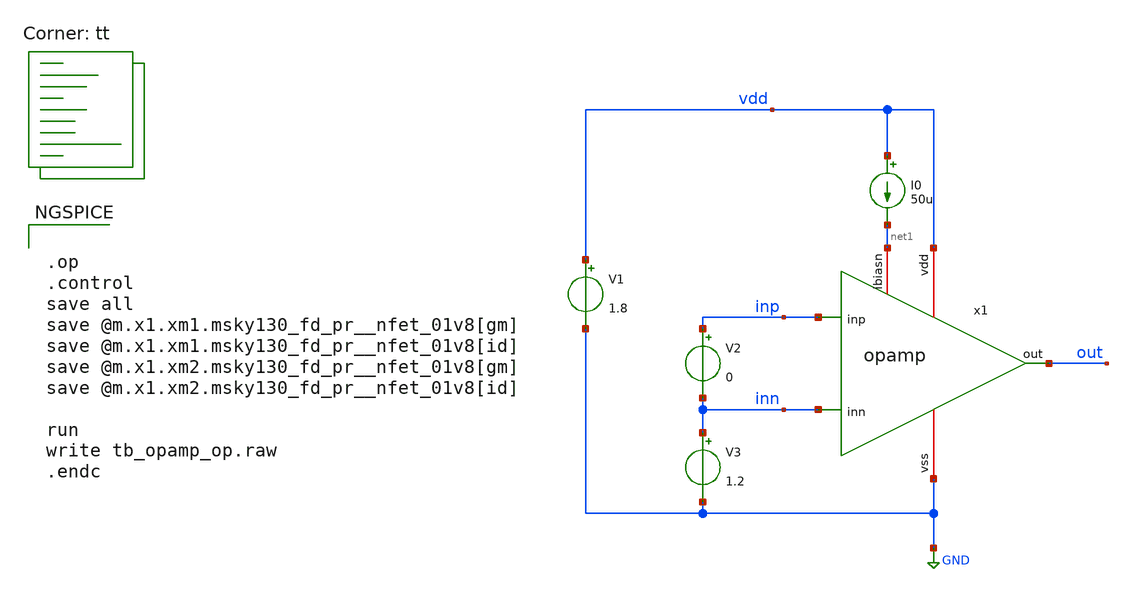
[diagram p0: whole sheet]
** sch_path: sky130A/HelloWorld/analog/schematic/tb_opamp_op.sch
**.subckt tb_opamp_op
x1 vdd out inp inn net1 GND opamp
V1 vdd GND 1.8
I0 vdd net1 50u
V2 inp inn 0
V3 inn GND 1.2
**** begin user architecture code
.lib $::SKYWATER_MODELS/sky130.lib.spice tt


.op
.control
save all
save @m.x1.xm1.msky130_fd_pr__nfet_01v8[gm]
save @m.x1.xm1.msky130_fd_pr__nfet_01v8[id]
save @m.x1.xm2.msky130_fd_pr__nfet_01v8[gm]
save @m.x1.xm2.msky130_fd_pr__nfet_01v8[id]

run
write tb_opamp_op.raw
.endc


**** end user architecture code
**.ends

* expanding   symbol:  opamp.sym # of pins=6
** sym_path: sky130A/HelloWorld/xschem/opamp.sym
** sch_path: sky130A/HelloWorld/xschem/opamp.sch
.subckt opamp vdd out inp inn ibiasn vss
*.ipin inn
*.ipin inp
*.iopin vdd
*.iopin vss
*.iopin ibiasn
*.opin out
XM1 pbias inn tail vss sky130_fd_pr__nfet_01v8 L=1 W=40 nf=1 ad='int((nf+1)/2) * W/nf * 0.29' as='int((nf+2)/2) * W/nf * 0.29'
+ pd='2*int((nf+1)/2) * (W/nf + 0.29)' ps='2*int((nf+2)/2) * (W/nf + 0.29)' nrd='0.29 / W' nrs='0.29 / W'
+ sa=0 sb=0 sd=0 mult=1 m=1
XM2 outz inp tail vss sky130_fd_pr__nfet_01v8 L=1 W=40 nf=1 ad='int((nf+1)/2) * W/nf * 0.29' as='int((nf+2)/2) * W/nf * 0.29'
+ pd='2*int((nf+1)/2) * (W/nf + 0.29)' ps='2*int((nf+2)/2) * (W/nf + 0.29)' nrd='0.29 / W' nrs='0.29 / W'
+ sa=0 sb=0 sd=0 mult=1 m=1
XM3 pbias pbias vdd vdd sky130_fd_pr__pfet_01v8 L=0.5 W=20 nf=1 ad='int((nf+1)/2) * W/nf * 0.29' as='int((nf+2)/2) * W/nf * 0.29'
+ pd='2*int((nf+1)/2) * (W/nf + 0.29)' ps='2*int((nf+2)/2) * (W/nf + 0.29)' nrd='0.29 / W' nrs='0.29 / W'
+ sa=0 sb=0 sd=0 mult=1 m=1
XM4 outz pbias vdd vdd sky130_fd_pr__pfet_01v8 L=0.5 W=20 nf=1 ad='int((nf+1)/2) * W/nf * 0.29' as='int((nf+2)/2) * W/nf * 0.29'
+ pd='2*int((nf+1)/2) * (W/nf + 0.29)' ps='2*int((nf+2)/2) * (W/nf + 0.29)' nrd='0.29 / W' nrs='0.29 / W'
+ sa=0 sb=0 sd=0 mult=1 m=1
XM5 out outz vdd vdd sky130_fd_pr__pfet_01v8 L=0.5 W=20 nf=1 ad='int((nf+1)/2) * W/nf * 0.29' as='int((nf+2)/2) * W/nf * 0.29'
+ pd='2*int((nf+1)/2) * (W/nf + 0.29)' ps='2*int((nf+2)/2) * (W/nf + 0.29)' nrd='0.29 / W' nrs='0.29 / W'
+ sa=0 sb=0 sd=0 mult=1 m=1
XM6[1] tail ibiasn vss vss sky130_fd_pr__nfet_01v8 L=1 W=40 nf=1 ad='int((nf+1)/2) * W/nf * 0.29' as='int((nf+2)/2) * W/nf * 0.29'
+ pd='2*int((nf+1)/2) * (W/nf + 0.29)' ps='2*int((nf+2)/2) * (W/nf + 0.29)' nrd='0.29 / W' nrs='0.29 / W'
+ sa=0 sb=0 sd=0 mult=1 m=1
XM6[0] tail ibiasn vss vss sky130_fd_pr__nfet_01v8 L=1 W=40 nf=1 ad='int((nf+1)/2) * W/nf * 0.29' as='int((nf+2)/2) * W/nf * 0.29'
+ pd='2*int((nf+1)/2) * (W/nf + 0.29)' ps='2*int((nf+2)/2) * (W/nf + 0.29)' nrd='0.29 / W' nrs='0.29 / W'
+ sa=0 sb=0 sd=0 mult=1 m=1
XM7 out ibiasn vss vss sky130_fd_pr__nfet_01v8 L=1 W=40 nf=1 ad='int((nf+1)/2) * W/nf * 0.29' as='int((nf+2)/2) * W/nf * 0.29'
+ pd='2*int((nf+1)/2) * (W/nf + 0.29)' ps='2*int((nf+2)/2) * (W/nf + 0.29)' nrd='0.29 / W' nrs='0.29 / W'
+ sa=0 sb=0 sd=0 mult=1 m=1
XM8 ibiasn ibiasn vss vss sky130_fd_pr__nfet_01v8 L=1 W=40 nf=1 ad='int((nf+1)/2) * W/nf * 0.29' as='int((nf+2)/2) * W/nf * 0.29'
+ pd='2*int((nf+1)/2) * (W/nf + 0.29)' ps='2*int((nf+2)/2) * (W/nf + 0.29)' nrd='0.29 / W' nrs='0.29 / W'
+ sa=0 sb=0 sd=0 mult=1 m=1
.ends

.GLOBAL GND
.end
